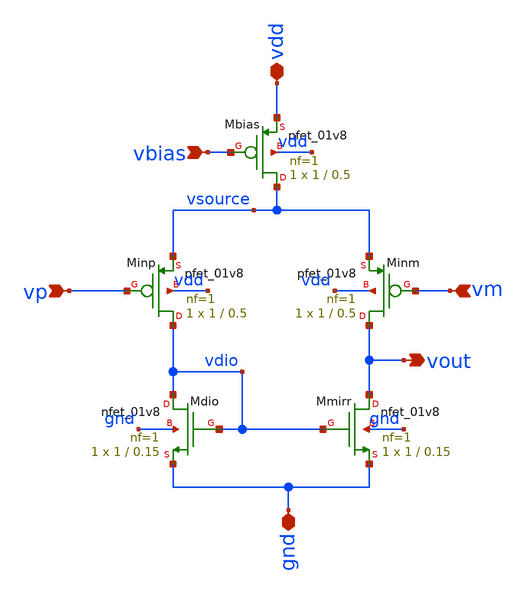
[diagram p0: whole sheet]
** sch_path: analog/klayout/production/final_merge_20260923/testbenches/cace/analog/xschem/amp_p.sch
**.subckt amp_p gnd vp vm vout vbias vdd
*.iopin gnd
*.ipin vp
*.ipin vm
*.opin vout
*.ipin vbias
*.iopin vdd
XMinm vout vm vsource vdd sky130_fd_pr__pfet_01v8 L=0.5 W=1 nf=1 ad='int((1 + 1)/2) * 1 / 1 * 0.29' as='int((1 + 2)/2) * 1 / 1 * 0.29'
+ pd='2*int((1 + 1)/2) * (1 / 1 + 0.29)' ps='2*int((1 + 2)/2) * (1 / 1 + 0.29)' nrd='0.29 / 1 ' nrs='0.29 / 1 '
+ sa=0 sb=0 sd=0 mult=1 m=1
XMinp vdio vp vsource vdd sky130_fd_pr__pfet_01v8 L=0.5 W=1 nf=1 ad='int((1 + 1)/2) * 1 / 1 * 0.29' as='int((1 + 2)/2) * 1 / 1 * 0.29'
+ pd='2*int((1 + 1)/2) * (1 / 1 + 0.29)' ps='2*int((1 + 2)/2) * (1 / 1 + 0.29)' nrd='0.29 / 1 ' nrs='0.29 / 1 '
+ sa=0 sb=0 sd=0 mult=1 m=1
XMdio vdio vdio gnd gnd sky130_fd_pr__nfet_01v8 L=0.15 W=1 nf=1 ad='int((1 + 1)/2) * 1 / 1 * 0.29' as='int((1 + 2)/2) * 1 / 1 * 0.29'
+ pd='2*int((1 + 1)/2) * (1 / 1 + 0.29)' ps='2*int((1 + 2)/2) * (1 / 1 + 0.29)' nrd='0.29 / 1 ' nrs='0.29 / 1 '
+ sa=0 sb=0 sd=0 mult=1 m=1
XMmirr vout vdio gnd gnd sky130_fd_pr__nfet_01v8 L=0.15 W=1 nf=1 ad='int((1 + 1)/2) * 1 / 1 * 0.29' as='int((1 + 2)/2) * 1 / 1 * 0.29'
+ pd='2*int((1 + 1)/2) * (1 / 1 + 0.29)' ps='2*int((1 + 2)/2) * (1 / 1 + 0.29)' nrd='0.29 / 1 ' nrs='0.29 / 1 '
+ sa=0 sb=0 sd=0 mult=1 m=1
XMbias vsource vbias vdd vdd sky130_fd_pr__pfet_01v8 L=0.5 W=1 nf=1 ad='int((1 + 1)/2) * 1 / 1 * 0.29'
+ as='int((1 + 2)/2) * 1 / 1 * 0.29' pd='2*int((1 + 1)/2) * (1 / 1 + 0.29)' ps='2*int((1 + 2)/2) * (1 / 1 + 0.29)'
+ nrd='0.29 / 1 ' nrs='0.29 / 1 ' sa=0 sb=0 sd=0 mult=1 m=1
**.ends
.end
